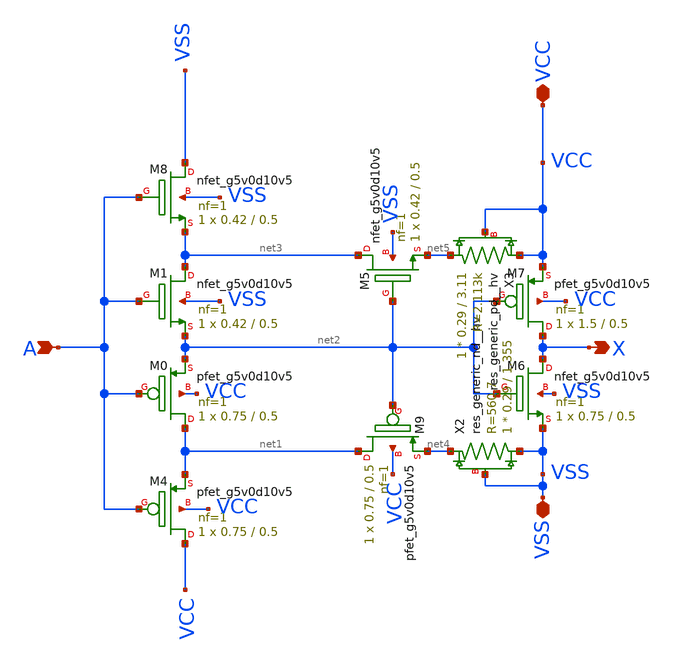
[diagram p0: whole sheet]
** sch_path: DISEÑO/ANALOGICO/V;SI/ST/xschem/schmitt_trigger.sch
**.subckt schmitt_trigger A X VSS VCC
*.ipin A
*.opin X
*.iopin VSS
*.iopin VCC
XM0 net1 A net2 VCC sky130_fd_pr__pfet_g5v0d10v5 L=0.5 W=0.75 nf=1 ad='int((nf+1)/2) * W/nf * 0.29' as='int((nf+2)/2) * W/nf * 0.29'
+ pd='2*int((nf+1)/2) * (W/nf + 0.29)' ps='2*int((nf+2)/2) * (W/nf + 0.29)' nrd='0.29 / W' nrs='0.29 / W'
+ sa=0 sb=0 sd=0 mult=1 m=1
XM1 net3 A net2 VSS sky130_fd_pr__nfet_g5v0d10v5 L=0.5 W=0.42 nf=1 ad='int((nf+1)/2) * W/nf * 0.29' as='int((nf+2)/2) * W/nf * 0.29'
+ pd='2*int((nf+1)/2) * (W/nf + 0.29)' ps='2*int((nf+2)/2) * (W/nf + 0.29)' nrd='0.29 / W' nrs='0.29 / W'
+ sa=0 sb=0 sd=0 mult=1 m=1
XM7 X net2 VCC VCC sky130_fd_pr__pfet_g5v0d10v5 L=0.5 W=1.5 nf=1 ad='int((nf+1)/2) * W/nf * 0.29' as='int((nf+2)/2) * W/nf * 0.29'
+ pd='2*int((nf+1)/2) * (W/nf + 0.29)' ps='2*int((nf+2)/2) * (W/nf + 0.29)' nrd='0.29 / W' nrs='0.29 / W'
+ sa=0 sb=0 sd=0 mult=1 m=1
XM6 X net2 VSS VSS sky130_fd_pr__nfet_g5v0d10v5 L=0.5 W=0.75 nf=1 ad='int((nf+1)/2) * W/nf * 0.29' as='int((nf+2)/2) * W/nf * 0.29'
+ pd='2*int((nf+1)/2) * (W/nf + 0.29)' ps='2*int((nf+2)/2) * (W/nf + 0.29)' nrd='0.29 / W' nrs='0.29 / W'
+ sa=0 sb=0 sd=0 mult=1 m=1
XM4 VCC A net1 VCC sky130_fd_pr__pfet_g5v0d10v5 L=0.5 W=0.75 nf=1 ad='int((nf+1)/2) * W/nf * 0.29' as='int((nf+2)/2) * W/nf * 0.29'
+ pd='2*int((nf+1)/2) * (W/nf + 0.29)' ps='2*int((nf+2)/2) * (W/nf + 0.29)' nrd='0.29 / W' nrs='0.29 / W'
+ sa=0 sb=0 sd=0 mult=1 m=1
XM5 net3 net2 net5 VSS sky130_fd_pr__nfet_g5v0d10v5 L=0.5 W=0.42 nf=1 ad='int((nf+1)/2) * W/nf * 0.29'
+ as='int((nf+2)/2) * W/nf * 0.29' pd='2*int((nf+1)/2) * (W/nf + 0.29)' ps='2*int((nf+2)/2) * (W/nf + 0.29)'
+ nrd='0.29 / W' nrs='0.29 / W' sa=0 sb=0 sd=0 mult=1 m=1
XM9 net1 net2 net4 VCC sky130_fd_pr__pfet_g5v0d10v5 L=0.5 W=0.75 nf=1 ad='int((nf+1)/2) * W/nf * 0.29'
+ as='int((nf+2)/2) * W/nf * 0.29' pd='2*int((nf+1)/2) * (W/nf + 0.29)' ps='2*int((nf+2)/2) * (W/nf + 0.29)'
+ nrd='0.29 / W' nrs='0.29 / W' sa=0 sb=0 sd=0 mult=1 m=1
XM8 VSS A net3 VSS sky130_fd_pr__nfet_g5v0d10v5 L=0.5 W=0.42 nf=1 ad='int((nf+1)/2) * W/nf * 0.29' as='int((nf+2)/2) * W/nf * 0.29'
+ pd='2*int((nf+1)/2) * (W/nf + 0.29)' ps='2*int((nf+2)/2) * (W/nf + 0.29)' nrd='0.29 / W' nrs='0.29 / W'
+ sa=0 sb=0 sd=0 mult=1 m=1
XX2 VSS net4 VSS sky130_fd_pr__res_generic_nd__hv W=0.29 L=1.355 mult=1 m=1
XX3 net5 VCC VCC sky130_fd_pr__res_generic_pd__hv W=0.29 L=3.11 mult=1 m=1
**.ends
.end
